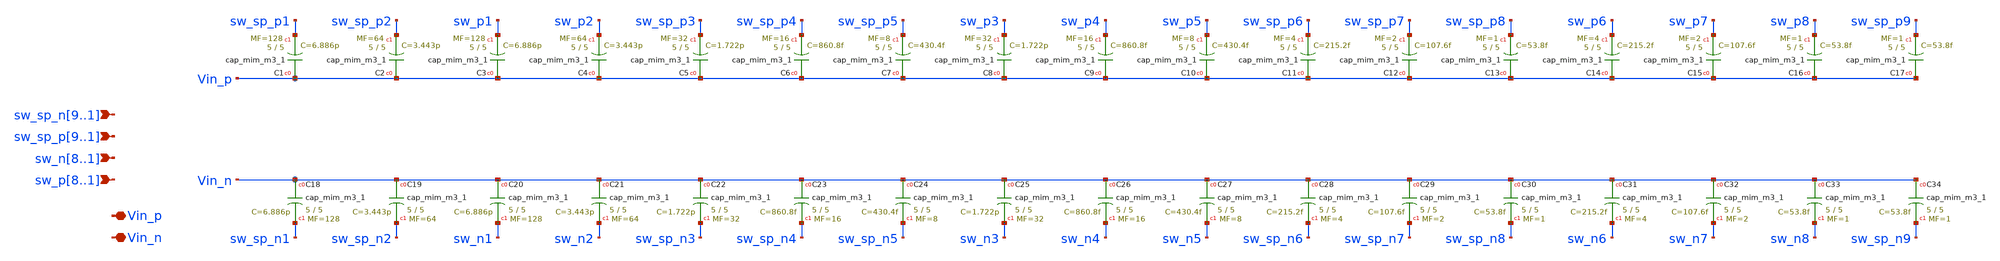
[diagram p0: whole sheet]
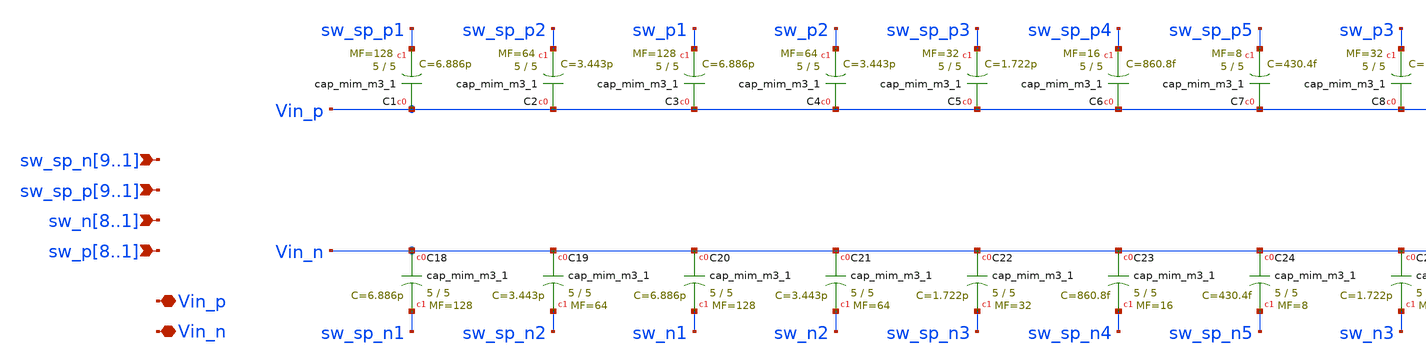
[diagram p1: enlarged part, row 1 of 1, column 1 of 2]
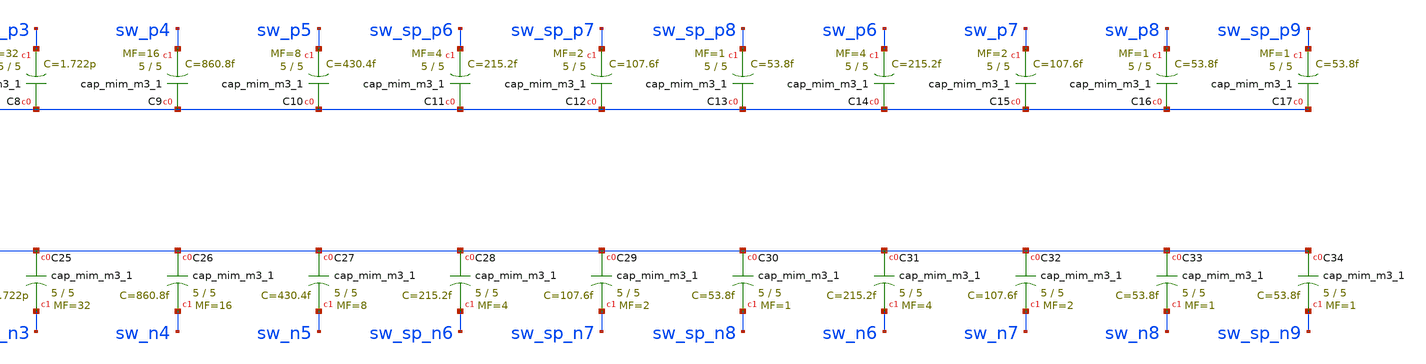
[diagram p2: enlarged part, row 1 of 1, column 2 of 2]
** sch_path: xschem/capacitor_array.sch
**.subckt capacitor_array
*+ sw_sp_n9,sw_sp_n8,sw_sp_n7,sw_sp_n6,sw_sp_n5,sw_sp_n4,sw_sp_n3,sw_sp_n2,sw_sp_n1 sw_sp_p9,sw_sp_p8,sw_sp_p7,sw_sp_p6,sw_sp_p5,sw_sp_p4,sw_sp_p3,sw_sp_p2,sw_sp_p1
*+ sw_n8,sw_n7,sw_n6,sw_n5,sw_n4,sw_n3,sw_n2,sw_n1 sw_p8,sw_p7,sw_p6,sw_p5,sw_p4,sw_p3,sw_p2,sw_p1 Vin_p Vin_n
*.ipin sw_sp_n9,sw_sp_n8,sw_sp_n7,sw_sp_n6,sw_sp_n5,sw_sp_n4,sw_sp_n3,sw_sp_n2,sw_sp_n1
*.ipin sw_sp_p9,sw_sp_p8,sw_sp_p7,sw_sp_p6,sw_sp_p5,sw_sp_p4,sw_sp_p3,sw_sp_p2,sw_sp_p1
*.ipin sw_n8,sw_n7,sw_n6,sw_n5,sw_n4,sw_n3,sw_n2,sw_n1
*.ipin sw_p8,sw_p7,sw_p6,sw_p5,sw_p4,sw_p3,sw_p2,sw_p1
*.iopin Vin_p
*.iopin Vin_n
XC1 Vin_p sw_sp_p1 sky130_fd_pr__cap_mim_m3_1 W=5 L=5 MF=128 m=128
XC2 Vin_p sw_sp_p2 sky130_fd_pr__cap_mim_m3_1 W=5 L=5 MF=64 m=64
XC3 Vin_p sw_p1 sky130_fd_pr__cap_mim_m3_1 W=5 L=5 MF=128 m=128
XC4 Vin_p sw_p2 sky130_fd_pr__cap_mim_m3_1 W=5 L=5 MF=64 m=64
XC5 Vin_p sw_sp_p3 sky130_fd_pr__cap_mim_m3_1 W=5 L=5 MF=32 m=32
XC6 Vin_p sw_sp_p4 sky130_fd_pr__cap_mim_m3_1 W=5 L=5 MF=16 m=16
XC7 Vin_p sw_sp_p5 sky130_fd_pr__cap_mim_m3_1 W=5 L=5 MF=8 m=8
XC8 Vin_p sw_p3 sky130_fd_pr__cap_mim_m3_1 W=5 L=5 MF=32 m=32
XC9 Vin_p sw_p4 sky130_fd_pr__cap_mim_m3_1 W=5 L=5 MF=16 m=16
XC10 Vin_p sw_p5 sky130_fd_pr__cap_mim_m3_1 W=5 L=5 MF=8 m=8
XC11 Vin_p sw_sp_p6 sky130_fd_pr__cap_mim_m3_1 W=5 L=5 MF=4 m=4
XC12 Vin_p sw_sp_p7 sky130_fd_pr__cap_mim_m3_1 W=5 L=5 MF=2 m=2
XC13 Vin_p sw_sp_p8 sky130_fd_pr__cap_mim_m3_1 W=5 L=5 MF=1 m=1
XC14 Vin_p sw_p6 sky130_fd_pr__cap_mim_m3_1 W=5 L=5 MF=4 m=4
XC15 Vin_p sw_p7 sky130_fd_pr__cap_mim_m3_1 W=5 L=5 MF=2 m=2
XC16 Vin_p sw_p8 sky130_fd_pr__cap_mim_m3_1 W=5 L=5 MF=1 m=1
XC17 Vin_p sw_sp_p9 sky130_fd_pr__cap_mim_m3_1 W=5 L=5 MF=1 m=1
XC18 Vin_n sw_sp_n1 sky130_fd_pr__cap_mim_m3_1 W=5 L=5 MF=128 m=128
XC19 Vin_n sw_sp_n2 sky130_fd_pr__cap_mim_m3_1 W=5 L=5 MF=64 m=64
XC20 Vin_n sw_n1 sky130_fd_pr__cap_mim_m3_1 W=5 L=5 MF=128 m=128
XC21 Vin_n sw_n2 sky130_fd_pr__cap_mim_m3_1 W=5 L=5 MF=64 m=64
XC22 Vin_n sw_sp_n3 sky130_fd_pr__cap_mim_m3_1 W=5 L=5 MF=32 m=32
XC23 Vin_n sw_sp_n4 sky130_fd_pr__cap_mim_m3_1 W=5 L=5 MF=16 m=16
XC24 Vin_n sw_sp_n5 sky130_fd_pr__cap_mim_m3_1 W=5 L=5 MF=8 m=8
XC25 Vin_n sw_n3 sky130_fd_pr__cap_mim_m3_1 W=5 L=5 MF=32 m=32
XC26 Vin_n sw_n4 sky130_fd_pr__cap_mim_m3_1 W=5 L=5 MF=16 m=16
XC27 Vin_n sw_n5 sky130_fd_pr__cap_mim_m3_1 W=5 L=5 MF=8 m=8
XC28 Vin_n sw_sp_n6 sky130_fd_pr__cap_mim_m3_1 W=5 L=5 MF=4 m=4
XC29 Vin_n sw_sp_n7 sky130_fd_pr__cap_mim_m3_1 W=5 L=5 MF=2 m=2
XC30 Vin_n sw_sp_n8 sky130_fd_pr__cap_mim_m3_1 W=5 L=5 MF=1 m=1
XC31 Vin_n sw_n6 sky130_fd_pr__cap_mim_m3_1 W=5 L=5 MF=4 m=4
XC32 Vin_n sw_n7 sky130_fd_pr__cap_mim_m3_1 W=5 L=5 MF=2 m=2
XC33 Vin_n sw_n8 sky130_fd_pr__cap_mim_m3_1 W=5 L=5 MF=1 m=1
XC34 Vin_n sw_sp_n9 sky130_fd_pr__cap_mim_m3_1 W=5 L=5 MF=1 m=1
**.ends
.end
